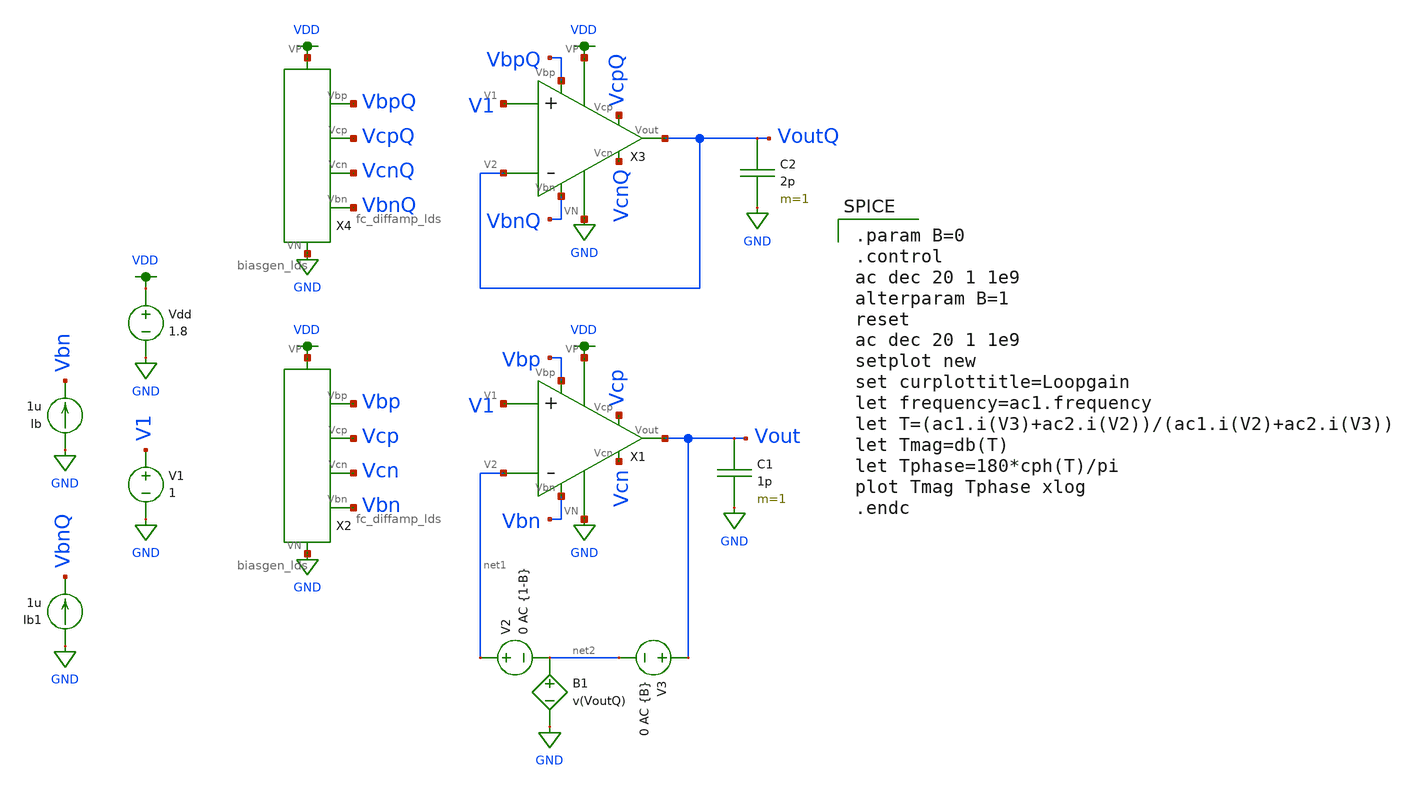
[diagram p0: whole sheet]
** sch_path: fc_diffamp_lg.sch
**.subckt fc_diffamp_lg
Vdd VDD GND 1.8
V1 V1 GND 1
Ib GND Vbn 1u
X1 V1 net1 VDD GND Vout Vbp Vbn Vcp Vcn fc_diffamp_lds
X2 VDD GND Vbn Vcn Vcp Vbp biasgen_lds
C1 Vout GND 1p m=1
Ib1 GND VbnQ 1u
X3 V1 VoutQ VDD GND VoutQ VbpQ VbnQ VcpQ VcnQ fc_diffamp_lds
X4 VDD GND VbnQ VcnQ VcpQ VbpQ biasgen_lds
C2 VoutQ GND 2p m=1
V2 net1 net2 0 AC {1-B}
V3 Vout net2 0 AC {B}
B1 net2 GND V=v(VoutQ)
**** begin user architecture code

.option wnflag=1
.lib ~/skywater/skywater-pdk/libraries/sky130_fd_pr_ngspice/latest/models/sky130.lib.spice tt


.param B=0
.control
ac dec 20 1 1e9
alterparam B=1
reset
ac dec 20 1 1e9
setplot new
set curplottitle=Loopgain
let frequency=ac1.frequency
let T=(ac1.i(V3)+ac2.i(V2))/(ac1.i(V2)+ac2.i(V3))
let Tmag=db(T)
let Tphase=180*cph(T)/pi
plot Tmag Tphase xlog
.endc

**** end user architecture code
**.ends

* expanding   symbol:  /home/madvlsi/Documents/mp3/fc_diffamp_lds.sym # of pins=9
** sym_path: fc_diffamp_lds.sym
** sch_path: fc_diffamp_lds.sch
.subckt fc_diffamp_lds V1 V2 VP VN Vout Vbp Vbn Vcp Vcn
*.ipin V1
*.ipin V2
*.opin Vout
*.iopin VN
*.iopin VP
*.ipin Vcp
*.ipin Vbp
*.ipin Vcn
*.ipin Vbn
XM1a net1 V1 net3 GND sky130_fd_pr__nfet_01v8 L=0.5 W=1.5 nf=1 ad='int((nf+1)/2) * W/nf * 0.29' as='int((nf+2)/2) * W/nf * 0.29'
+ pd='2*int((nf+1)/2) * (W/nf + 0.29)' ps='2*int((nf+2)/2) * (W/nf + 0.29)' nrd='0.29 / W' nrs='0.29 / W'
+ sa=0 sb=0 sd=0 mult=1 m=1
XM2a net1 V2 net2 GND sky130_fd_pr__nfet_01v8 L=0.5 W=1.5 nf=1 ad='int((nf+1)/2) * W/nf * 0.29' as='int((nf+2)/2) * W/nf * 0.29'
+ pd='2*int((nf+1)/2) * (W/nf + 0.29)' ps='2*int((nf+2)/2) * (W/nf + 0.29)' nrd='0.29 / W' nrs='0.29 / W'
+ sa=0 sb=0 sd=0 mult=1 m=1
XM2b net2 V2 net1 GND sky130_fd_pr__nfet_01v8 L=0.5 W=1.5 nf=1 ad='int((nf+1)/2) * W/nf * 0.29' as='int((nf+2)/2) * W/nf * 0.29'
+ pd='2*int((nf+1)/2) * (W/nf + 0.29)' ps='2*int((nf+2)/2) * (W/nf + 0.29)' nrd='0.29 / W' nrs='0.29 / W'
+ sa=0 sb=0 sd=0 mult=1 m=1
XM1b net3 V1 net1 GND sky130_fd_pr__nfet_01v8 L=0.5 W=1.5 nf=1 ad='int((nf+1)/2) * W/nf * 0.29' as='int((nf+2)/2) * W/nf * 0.29'
+ pd='2*int((nf+1)/2) * (W/nf + 0.29)' ps='2*int((nf+2)/2) * (W/nf + 0.29)' nrd='0.29 / W' nrs='0.29 / W'
+ sa=0 sb=0 sd=0 mult=1 m=1
XM1c net1 V1 net3 GND sky130_fd_pr__nfet_01v8 L=0.5 W=1.5 nf=1 ad='int((nf+1)/2) * W/nf * 0.29' as='int((nf+2)/2) * W/nf * 0.29'
+ pd='2*int((nf+1)/2) * (W/nf + 0.29)' ps='2*int((nf+2)/2) * (W/nf + 0.29)' nrd='0.29 / W' nrs='0.29 / W'
+ sa=0 sb=0 sd=0 mult=1 m=1
XM2c net1 V2 net2 GND sky130_fd_pr__nfet_01v8 L=0.5 W=1.5 nf=1 ad='int((nf+1)/2) * W/nf * 0.29' as='int((nf+2)/2) * W/nf * 0.29'
+ pd='2*int((nf+1)/2) * (W/nf + 0.29)' ps='2*int((nf+2)/2) * (W/nf + 0.29)' nrd='0.29 / W' nrs='0.29 / W'
+ sa=0 sb=0 sd=0 mult=1 m=1
XM2d net2 V2 net1 GND sky130_fd_pr__nfet_01v8 L=0.5 W=1.5 nf=1 ad='int((nf+1)/2) * W/nf * 0.29' as='int((nf+2)/2) * W/nf * 0.29'
+ pd='2*int((nf+1)/2) * (W/nf + 0.29)' ps='2*int((nf+2)/2) * (W/nf + 0.29)' nrd='0.29 / W' nrs='0.29 / W'
+ sa=0 sb=0 sd=0 mult=1 m=1
XM1d net3 V1 net1 GND sky130_fd_pr__nfet_01v8 L=0.5 W=1.5 nf=1 ad='int((nf+1)/2) * W/nf * 0.29' as='int((nf+2)/2) * W/nf * 0.29'
+ pd='2*int((nf+1)/2) * (W/nf + 0.29)' ps='2*int((nf+2)/2) * (W/nf + 0.29)' nrd='0.29 / W' nrs='0.29 / W'
+ sa=0 sb=0 sd=0 mult=1 m=1
XM11a net1 Vbn VN GND sky130_fd_pr__nfet_01v8 L=0.5 W=1.5 nf=1 ad='int((nf+1)/2) * W/nf * 0.29' as='int((nf+2)/2) * W/nf * 0.29'
+ pd='2*int((nf+1)/2) * (W/nf + 0.29)' ps='2*int((nf+2)/2) * (W/nf + 0.29)' nrd='0.29 / W' nrs='0.29 / W'
+ sa=0 sb=0 sd=0 mult=1 m=1
XM12a VN Vbn Vbn GND sky130_fd_pr__nfet_01v8 L=0.5 W=1.5 nf=1 ad='int((nf+1)/2) * W/nf * 0.29' as='int((nf+2)/2) * W/nf * 0.29'
+ pd='2*int((nf+1)/2) * (W/nf + 0.29)' ps='2*int((nf+2)/2) * (W/nf + 0.29)' nrd='0.29 / W' nrs='0.29 / W'
+ sa=0 sb=0 sd=0 mult=1 m=1
XM12b Vbn Vbn VN GND sky130_fd_pr__nfet_01v8 L=0.5 W=1.5 nf=1 ad='int((nf+1)/2) * W/nf * 0.29' as='int((nf+2)/2) * W/nf * 0.29'
+ pd='2*int((nf+1)/2) * (W/nf + 0.29)' ps='2*int((nf+2)/2) * (W/nf + 0.29)' nrd='0.29 / W' nrs='0.29 / W'
+ sa=0 sb=0 sd=0 mult=1 m=1
XM11b VN Vbn net1 GND sky130_fd_pr__nfet_01v8 L=0.5 W=1.5 nf=1 ad='int((nf+1)/2) * W/nf * 0.29' as='int((nf+2)/2) * W/nf * 0.29'
+ pd='2*int((nf+1)/2) * (W/nf + 0.29)' ps='2*int((nf+2)/2) * (W/nf + 0.29)' nrd='0.29 / W' nrs='0.29 / W'
+ sa=0 sb=0 sd=0 mult=1 m=1
XM11c net1 Vbn VN GND sky130_fd_pr__nfet_01v8 L=0.5 W=1.5 nf=1 ad='int((nf+1)/2) * W/nf * 0.29' as='int((nf+2)/2) * W/nf * 0.29'
+ pd='2*int((nf+1)/2) * (W/nf + 0.29)' ps='2*int((nf+2)/2) * (W/nf + 0.29)' nrd='0.29 / W' nrs='0.29 / W'
+ sa=0 sb=0 sd=0 mult=1 m=1
XM12c VN Vbn Vbn GND sky130_fd_pr__nfet_01v8 L=0.5 W=1.5 nf=1 ad='int((nf+1)/2) * W/nf * 0.29' as='int((nf+2)/2) * W/nf * 0.29'
+ pd='2*int((nf+1)/2) * (W/nf + 0.29)' ps='2*int((nf+2)/2) * (W/nf + 0.29)' nrd='0.29 / W' nrs='0.29 / W'
+ sa=0 sb=0 sd=0 mult=1 m=1
XM12d Vbn Vbn VN GND sky130_fd_pr__nfet_01v8 L=0.5 W=1.5 nf=1 ad='int((nf+1)/2) * W/nf * 0.29' as='int((nf+2)/2) * W/nf * 0.29'
+ pd='2*int((nf+1)/2) * (W/nf + 0.29)' ps='2*int((nf+2)/2) * (W/nf + 0.29)' nrd='0.29 / W' nrs='0.29 / W'
+ sa=0 sb=0 sd=0 mult=1 m=1
XM11d VN Vbn net1 GND sky130_fd_pr__nfet_01v8 L=0.5 W=1.5 nf=1 ad='int((nf+1)/2) * W/nf * 0.29' as='int((nf+2)/2) * W/nf * 0.29'
+ pd='2*int((nf+1)/2) * (W/nf + 0.29)' ps='2*int((nf+2)/2) * (W/nf + 0.29)' nrd='0.29 / W' nrs='0.29 / W'
+ sa=0 sb=0 sd=0 mult=1 m=1
XM9a net4 Vcn net8 GND sky130_fd_pr__nfet_01v8 L=0.5 W=3 nf=1 ad='int((nf+1)/2) * W/nf * 0.29' as='int((nf+2)/2) * W/nf * 0.29'
+ pd='2*int((nf+1)/2) * (W/nf + 0.29)' ps='2*int((nf+2)/2) * (W/nf + 0.29)' nrd='0.29 / W' nrs='0.29 / W'
+ sa=0 sb=0 sd=0 mult=1 m=1
XM7a net4 net8 VN GND sky130_fd_pr__nfet_01v8 L=0.5 W=3 nf=1 ad='int((nf+1)/2) * W/nf * 0.29' as='int((nf+2)/2) * W/nf * 0.29'
+ pd='2*int((nf+1)/2) * (W/nf + 0.29)' ps='2*int((nf+2)/2) * (W/nf + 0.29)' nrd='0.29 / W' nrs='0.29 / W'
+ sa=0 sb=0 sd=0 mult=1 m=1
XM8a VN net8 net5 GND sky130_fd_pr__nfet_01v8 L=0.5 W=3 nf=1 ad='int((nf+1)/2) * W/nf * 0.29' as='int((nf+2)/2) * W/nf * 0.29'
+ pd='2*int((nf+1)/2) * (W/nf + 0.29)' ps='2*int((nf+2)/2) * (W/nf + 0.29)' nrd='0.29 / W' nrs='0.29 / W'
+ sa=0 sb=0 sd=0 mult=1 m=1
XM10a Vout Vcn net5 GND sky130_fd_pr__nfet_01v8 L=0.5 W=3 nf=1 ad='int((nf+1)/2) * W/nf * 0.29' as='int((nf+2)/2) * W/nf * 0.29'
+ pd='2*int((nf+1)/2) * (W/nf + 0.29)' ps='2*int((nf+2)/2) * (W/nf + 0.29)' nrd='0.29 / W' nrs='0.29 / W'
+ sa=0 sb=0 sd=0 mult=1 m=1
XM10b net6 Vcn Vout GND sky130_fd_pr__nfet_01v8 L=0.5 W=3 nf=1 ad='int((nf+1)/2) * W/nf * 0.29' as='int((nf+2)/2) * W/nf * 0.29'
+ pd='2*int((nf+1)/2) * (W/nf + 0.29)' ps='2*int((nf+2)/2) * (W/nf + 0.29)' nrd='0.29 / W' nrs='0.29 / W'
+ sa=0 sb=0 sd=0 mult=1 m=1
XM9b net8 Vcn net7 GND sky130_fd_pr__nfet_01v8 L=0.5 W=3 nf=1 ad='int((nf+1)/2) * W/nf * 0.29' as='int((nf+2)/2) * W/nf * 0.29'
+ pd='2*int((nf+1)/2) * (W/nf + 0.29)' ps='2*int((nf+2)/2) * (W/nf + 0.29)' nrd='0.29 / W' nrs='0.29 / W'
+ sa=0 sb=0 sd=0 mult=1 m=1
XM7b VN net8 net7 GND sky130_fd_pr__nfet_01v8 L=0.5 W=3 nf=1 ad='int((nf+1)/2) * W/nf * 0.29' as='int((nf+2)/2) * W/nf * 0.29'
+ pd='2*int((nf+1)/2) * (W/nf + 0.29)' ps='2*int((nf+2)/2) * (W/nf + 0.29)' nrd='0.29 / W' nrs='0.29 / W'
+ sa=0 sb=0 sd=0 mult=1 m=1
XM8b net6 net8 VN GND sky130_fd_pr__nfet_01v8 L=0.5 W=3 nf=1 ad='int((nf+1)/2) * W/nf * 0.29' as='int((nf+2)/2) * W/nf * 0.29'
+ pd='2*int((nf+1)/2) * (W/nf + 0.29)' ps='2*int((nf+2)/2) * (W/nf + 0.29)' nrd='0.29 / W' nrs='0.29 / W'
+ sa=0 sb=0 sd=0 mult=1 m=1
XM9c net9 Vcn net8 GND sky130_fd_pr__nfet_01v8 L=0.5 W=3 nf=1 ad='int((nf+1)/2) * W/nf * 0.29' as='int((nf+2)/2) * W/nf * 0.29'
+ pd='2*int((nf+1)/2) * (W/nf + 0.29)' ps='2*int((nf+2)/2) * (W/nf + 0.29)' nrd='0.29 / W' nrs='0.29 / W'
+ sa=0 sb=0 sd=0 mult=1 m=1
XM7c net9 net8 VN GND sky130_fd_pr__nfet_01v8 L=0.5 W=3 nf=1 ad='int((nf+1)/2) * W/nf * 0.29' as='int((nf+2)/2) * W/nf * 0.29'
+ pd='2*int((nf+1)/2) * (W/nf + 0.29)' ps='2*int((nf+2)/2) * (W/nf + 0.29)' nrd='0.29 / W' nrs='0.29 / W'
+ sa=0 sb=0 sd=0 mult=1 m=1
XM8c VN net8 net10 GND sky130_fd_pr__nfet_01v8 L=0.5 W=3 nf=1 ad='int((nf+1)/2) * W/nf * 0.29' as='int((nf+2)/2) * W/nf * 0.29'
+ pd='2*int((nf+1)/2) * (W/nf + 0.29)' ps='2*int((nf+2)/2) * (W/nf + 0.29)' nrd='0.29 / W' nrs='0.29 / W'
+ sa=0 sb=0 sd=0 mult=1 m=1
XM10c Vout Vcn net10 GND sky130_fd_pr__nfet_01v8 L=0.5 W=3 nf=1 ad='int((nf+1)/2) * W/nf * 0.29' as='int((nf+2)/2) * W/nf * 0.29'
+ pd='2*int((nf+1)/2) * (W/nf + 0.29)' ps='2*int((nf+2)/2) * (W/nf + 0.29)' nrd='0.29 / W' nrs='0.29 / W'
+ sa=0 sb=0 sd=0 mult=1 m=1
XM10d net11 Vcn Vout GND sky130_fd_pr__nfet_01v8 L=0.5 W=3 nf=1 ad='int((nf+1)/2) * W/nf * 0.29' as='int((nf+2)/2) * W/nf * 0.29'
+ pd='2*int((nf+1)/2) * (W/nf + 0.29)' ps='2*int((nf+2)/2) * (W/nf + 0.29)' nrd='0.29 / W' nrs='0.29 / W'
+ sa=0 sb=0 sd=0 mult=1 m=1
XM9d net8 Vcn net12 GND sky130_fd_pr__nfet_01v8 L=0.5 W=3 nf=1 ad='int((nf+1)/2) * W/nf * 0.29' as='int((nf+2)/2) * W/nf * 0.29'
+ pd='2*int((nf+1)/2) * (W/nf + 0.29)' ps='2*int((nf+2)/2) * (W/nf + 0.29)' nrd='0.29 / W' nrs='0.29 / W'
+ sa=0 sb=0 sd=0 mult=1 m=1
XM7d VN net8 net12 GND sky130_fd_pr__nfet_01v8 L=0.5 W=3 nf=1 ad='int((nf+1)/2) * W/nf * 0.29' as='int((nf+2)/2) * W/nf * 0.29'
+ pd='2*int((nf+1)/2) * (W/nf + 0.29)' ps='2*int((nf+2)/2) * (W/nf + 0.29)' nrd='0.29 / W' nrs='0.29 / W'
+ sa=0 sb=0 sd=0 mult=1 m=1
XM8d net11 net8 VN GND sky130_fd_pr__nfet_01v8 L=0.5 W=3 nf=1 ad='int((nf+1)/2) * W/nf * 0.29' as='int((nf+2)/2) * W/nf * 0.29'
+ pd='2*int((nf+1)/2) * (W/nf + 0.29)' ps='2*int((nf+2)/2) * (W/nf + 0.29)' nrd='0.29 / W' nrs='0.29 / W'
+ sa=0 sb=0 sd=0 mult=1 m=1
XM5a net8 Vcp net3 VDD sky130_fd_pr__pfet_01v8 L=0.5 W=3 nf=1 ad='int((nf+1)/2) * W/nf * 0.29' as='int((nf+2)/2) * W/nf * 0.29'
+ pd='2*int((nf+1)/2) * (W/nf + 0.29)' ps='2*int((nf+2)/2) * (W/nf + 0.29)' nrd='0.29 / W' nrs='0.29 / W'
+ sa=0 sb=0 sd=0 mult=1 m=1
XM5b net3 Vcp net8 VDD sky130_fd_pr__pfet_01v8 L=0.5 W=3 nf=1 ad='int((nf+1)/2) * W/nf * 0.29' as='int((nf+2)/2) * W/nf * 0.29'
+ pd='2*int((nf+1)/2) * (W/nf + 0.29)' ps='2*int((nf+2)/2) * (W/nf + 0.29)' nrd='0.29 / W' nrs='0.29 / W'
+ sa=0 sb=0 sd=0 mult=1 m=1
XM5c net8 Vcp net3 VDD sky130_fd_pr__pfet_01v8 L=0.5 W=3 nf=1 ad='int((nf+1)/2) * W/nf * 0.29' as='int((nf+2)/2) * W/nf * 0.29'
+ pd='2*int((nf+1)/2) * (W/nf + 0.29)' ps='2*int((nf+2)/2) * (W/nf + 0.29)' nrd='0.29 / W' nrs='0.29 / W'
+ sa=0 sb=0 sd=0 mult=1 m=1
XM5d net3 Vcp net8 VDD sky130_fd_pr__pfet_01v8 L=0.5 W=3 nf=1 ad='int((nf+1)/2) * W/nf * 0.29' as='int((nf+2)/2) * W/nf * 0.29'
+ pd='2*int((nf+1)/2) * (W/nf + 0.29)' ps='2*int((nf+2)/2) * (W/nf + 0.29)' nrd='0.29 / W' nrs='0.29 / W'
+ sa=0 sb=0 sd=0 mult=1 m=1
XM6a net2 Vcp Vout VDD sky130_fd_pr__pfet_01v8 L=0.5 W=3 nf=1 ad='int((nf+1)/2) * W/nf * 0.29' as='int((nf+2)/2) * W/nf * 0.29'
+ pd='2*int((nf+1)/2) * (W/nf + 0.29)' ps='2*int((nf+2)/2) * (W/nf + 0.29)' nrd='0.29 / W' nrs='0.29 / W'
+ sa=0 sb=0 sd=0 mult=1 m=1
XM6b Vout Vcp net2 VDD sky130_fd_pr__pfet_01v8 L=0.5 W=3 nf=1 ad='int((nf+1)/2) * W/nf * 0.29' as='int((nf+2)/2) * W/nf * 0.29'
+ pd='2*int((nf+1)/2) * (W/nf + 0.29)' ps='2*int((nf+2)/2) * (W/nf + 0.29)' nrd='0.29 / W' nrs='0.29 / W'
+ sa=0 sb=0 sd=0 mult=1 m=1
XM6c net2 Vcp Vout VDD sky130_fd_pr__pfet_01v8 L=0.5 W=3 nf=1 ad='int((nf+1)/2) * W/nf * 0.29' as='int((nf+2)/2) * W/nf * 0.29'
+ pd='2*int((nf+1)/2) * (W/nf + 0.29)' ps='2*int((nf+2)/2) * (W/nf + 0.29)' nrd='0.29 / W' nrs='0.29 / W'
+ sa=0 sb=0 sd=0 mult=1 m=1
XM6d Vout Vcp net2 VDD sky130_fd_pr__pfet_01v8 L=0.5 W=3 nf=1 ad='int((nf+1)/2) * W/nf * 0.29' as='int((nf+2)/2) * W/nf * 0.29'
+ pd='2*int((nf+1)/2) * (W/nf + 0.29)' ps='2*int((nf+2)/2) * (W/nf + 0.29)' nrd='0.29 / W' nrs='0.29 / W'
+ sa=0 sb=0 sd=0 mult=1 m=1
XM3a VP Vbp net3 VDD sky130_fd_pr__pfet_01v8 L=0.5 W=3 nf=1 ad='int((nf+1)/2) * W/nf * 0.29' as='int((nf+2)/2) * W/nf * 0.29'
+ pd='2*int((nf+1)/2) * (W/nf + 0.29)' ps='2*int((nf+2)/2) * (W/nf + 0.29)' nrd='0.29 / W' nrs='0.29 / W'
+ sa=0 sb=0 sd=0 mult=1 m=1
XM3b net3 Vbp VP VDD sky130_fd_pr__pfet_01v8 L=0.5 W=3 nf=1 ad='int((nf+1)/2) * W/nf * 0.29' as='int((nf+2)/2) * W/nf * 0.29'
+ pd='2*int((nf+1)/2) * (W/nf + 0.29)' ps='2*int((nf+2)/2) * (W/nf + 0.29)' nrd='0.29 / W' nrs='0.29 / W'
+ sa=0 sb=0 sd=0 mult=1 m=1
XM3c VP Vbp net3 VDD sky130_fd_pr__pfet_01v8 L=0.5 W=3 nf=1 ad='int((nf+1)/2) * W/nf * 0.29' as='int((nf+2)/2) * W/nf * 0.29'
+ pd='2*int((nf+1)/2) * (W/nf + 0.29)' ps='2*int((nf+2)/2) * (W/nf + 0.29)' nrd='0.29 / W' nrs='0.29 / W'
+ sa=0 sb=0 sd=0 mult=1 m=1
XM3d net3 Vbp VP VDD sky130_fd_pr__pfet_01v8 L=0.5 W=3 nf=1 ad='int((nf+1)/2) * W/nf * 0.29' as='int((nf+2)/2) * W/nf * 0.29'
+ pd='2*int((nf+1)/2) * (W/nf + 0.29)' ps='2*int((nf+2)/2) * (W/nf + 0.29)' nrd='0.29 / W' nrs='0.29 / W'
+ sa=0 sb=0 sd=0 mult=1 m=1
XM4a net2 Vbp VP VDD sky130_fd_pr__pfet_01v8 L=0.5 W=3 nf=1 ad='int((nf+1)/2) * W/nf * 0.29' as='int((nf+2)/2) * W/nf * 0.29'
+ pd='2*int((nf+1)/2) * (W/nf + 0.29)' ps='2*int((nf+2)/2) * (W/nf + 0.29)' nrd='0.29 / W' nrs='0.29 / W'
+ sa=0 sb=0 sd=0 mult=1 m=1
XM4b VP Vbp net2 VDD sky130_fd_pr__pfet_01v8 L=0.5 W=3 nf=1 ad='int((nf+1)/2) * W/nf * 0.29' as='int((nf+2)/2) * W/nf * 0.29'
+ pd='2*int((nf+1)/2) * (W/nf + 0.29)' ps='2*int((nf+2)/2) * (W/nf + 0.29)' nrd='0.29 / W' nrs='0.29 / W'
+ sa=0 sb=0 sd=0 mult=1 m=1
XM4c net2 Vbp VP VDD sky130_fd_pr__pfet_01v8 L=0.5 W=3 nf=1 ad='int((nf+1)/2) * W/nf * 0.29' as='int((nf+2)/2) * W/nf * 0.29'
+ pd='2*int((nf+1)/2) * (W/nf + 0.29)' ps='2*int((nf+2)/2) * (W/nf + 0.29)' nrd='0.29 / W' nrs='0.29 / W'
+ sa=0 sb=0 sd=0 mult=1 m=1
XM4d VP Vbp net2 VDD sky130_fd_pr__pfet_01v8 L=0.5 W=3 nf=1 ad='int((nf+1)/2) * W/nf * 0.29' as='int((nf+2)/2) * W/nf * 0.29'
+ pd='2*int((nf+1)/2) * (W/nf + 0.29)' ps='2*int((nf+2)/2) * (W/nf + 0.29)' nrd='0.29 / W' nrs='0.29 / W'
+ sa=0 sb=0 sd=0 mult=1 m=1
XM13 VN VN net3 GND sky130_fd_pr__nfet_01v8 L=0.5 W=1.5 nf=1 ad='int((nf+1)/2) * W/nf * 0.29' as='int((nf+2)/2) * W/nf * 0.29'
+ pd='2*int((nf+1)/2) * (W/nf + 0.29)' ps='2*int((nf+2)/2) * (W/nf + 0.29)' nrd='0.29 / W' nrs='0.29 / W'
+ sa=0 sb=0 sd=0 mult=1 m=1
XM15 VN VN net8 GND sky130_fd_pr__nfet_01v8 L=0.5 W=3 nf=1 ad='int((nf+1)/2) * W/nf * 0.29' as='int((nf+2)/2) * W/nf * 0.29'
+ pd='2*int((nf+1)/2) * (W/nf + 0.29)' ps='2*int((nf+2)/2) * (W/nf + 0.29)' nrd='0.29 / W' nrs='0.29 / W'
+ sa=0 sb=0 sd=0 mult=1 m=1
XM17 Vbn VN VN GND sky130_fd_pr__nfet_01v8 L=0.5 W=1.5 nf=1 ad='int((nf+1)/2) * W/nf * 0.29' as='int((nf+2)/2) * W/nf * 0.29'
+ pd='2*int((nf+1)/2) * (W/nf + 0.29)' ps='2*int((nf+2)/2) * (W/nf + 0.29)' nrd='0.29 / W' nrs='0.29 / W'
+ sa=0 sb=0 sd=0 mult=1 m=1
XM18 net8 VN VN GND sky130_fd_pr__nfet_01v8 L=0.5 W=3 nf=1 ad='int((nf+1)/2) * W/nf * 0.29' as='int((nf+2)/2) * W/nf * 0.29'
+ pd='2*int((nf+1)/2) * (W/nf + 0.29)' ps='2*int((nf+2)/2) * (W/nf + 0.29)' nrd='0.29 / W' nrs='0.29 / W'
+ sa=0 sb=0 sd=0 mult=1 m=1
XM19 VP VP net8 VDD sky130_fd_pr__pfet_01v8 L=0.5 W=3 nf=1 ad='int((nf+1)/2) * W/nf * 0.29' as='int((nf+2)/2) * W/nf * 0.29'
+ pd='2*int((nf+1)/2) * (W/nf + 0.29)' ps='2*int((nf+2)/2) * (W/nf + 0.29)' nrd='0.29 / W' nrs='0.29 / W'
+ sa=0 sb=0 sd=0 mult=1 m=1
XM20 net8 VP VP VDD sky130_fd_pr__pfet_01v8 L=0.5 W=3 nf=1 ad='int((nf+1)/2) * W/nf * 0.29' as='int((nf+2)/2) * W/nf * 0.29'
+ pd='2*int((nf+1)/2) * (W/nf + 0.29)' ps='2*int((nf+2)/2) * (W/nf + 0.29)' nrd='0.29 / W' nrs='0.29 / W'
+ sa=0 sb=0 sd=0 mult=1 m=1
XM1e net1 V1 net3 GND sky130_fd_pr__nfet_01v8 L=0.5 W=1.5 nf=1 ad='int((nf+1)/2) * W/nf * 0.29' as='int((nf+2)/2) * W/nf * 0.29'
+ pd='2*int((nf+1)/2) * (W/nf + 0.29)' ps='2*int((nf+2)/2) * (W/nf + 0.29)' nrd='0.29 / W' nrs='0.29 / W'
+ sa=0 sb=0 sd=0 mult=1 m=1
XM2e net1 V2 net2 GND sky130_fd_pr__nfet_01v8 L=0.5 W=1.5 nf=1 ad='int((nf+1)/2) * W/nf * 0.29' as='int((nf+2)/2) * W/nf * 0.29'
+ pd='2*int((nf+1)/2) * (W/nf + 0.29)' ps='2*int((nf+2)/2) * (W/nf + 0.29)' nrd='0.29 / W' nrs='0.29 / W'
+ sa=0 sb=0 sd=0 mult=1 m=1
XM2f net2 V2 net1 GND sky130_fd_pr__nfet_01v8 L=0.5 W=1.5 nf=1 ad='int((nf+1)/2) * W/nf * 0.29' as='int((nf+2)/2) * W/nf * 0.29'
+ pd='2*int((nf+1)/2) * (W/nf + 0.29)' ps='2*int((nf+2)/2) * (W/nf + 0.29)' nrd='0.29 / W' nrs='0.29 / W'
+ sa=0 sb=0 sd=0 mult=1 m=1
XM1f net3 V1 net1 GND sky130_fd_pr__nfet_01v8 L=0.5 W=1.5 nf=1 ad='int((nf+1)/2) * W/nf * 0.29' as='int((nf+2)/2) * W/nf * 0.29'
+ pd='2*int((nf+1)/2) * (W/nf + 0.29)' ps='2*int((nf+2)/2) * (W/nf + 0.29)' nrd='0.29 / W' nrs='0.29 / W'
+ sa=0 sb=0 sd=0 mult=1 m=1
XM1g net1 V1 net3 GND sky130_fd_pr__nfet_01v8 L=0.5 W=1.5 nf=1 ad='int((nf+1)/2) * W/nf * 0.29' as='int((nf+2)/2) * W/nf * 0.29'
+ pd='2*int((nf+1)/2) * (W/nf + 0.29)' ps='2*int((nf+2)/2) * (W/nf + 0.29)' nrd='0.29 / W' nrs='0.29 / W'
+ sa=0 sb=0 sd=0 mult=1 m=1
XM2g net1 V2 net2 GND sky130_fd_pr__nfet_01v8 L=0.5 W=1.5 nf=1 ad='int((nf+1)/2) * W/nf * 0.29' as='int((nf+2)/2) * W/nf * 0.29'
+ pd='2*int((nf+1)/2) * (W/nf + 0.29)' ps='2*int((nf+2)/2) * (W/nf + 0.29)' nrd='0.29 / W' nrs='0.29 / W'
+ sa=0 sb=0 sd=0 mult=1 m=1
XM2h net2 V2 net1 GND sky130_fd_pr__nfet_01v8 L=0.5 W=1.5 nf=1 ad='int((nf+1)/2) * W/nf * 0.29' as='int((nf+2)/2) * W/nf * 0.29'
+ pd='2*int((nf+1)/2) * (W/nf + 0.29)' ps='2*int((nf+2)/2) * (W/nf + 0.29)' nrd='0.29 / W' nrs='0.29 / W'
+ sa=0 sb=0 sd=0 mult=1 m=1
XM1h net3 V1 net1 GND sky130_fd_pr__nfet_01v8 L=0.5 W=1.5 nf=1 ad='int((nf+1)/2) * W/nf * 0.29' as='int((nf+2)/2) * W/nf * 0.29'
+ pd='2*int((nf+1)/2) * (W/nf + 0.29)' ps='2*int((nf+2)/2) * (W/nf + 0.29)' nrd='0.29 / W' nrs='0.29 / W'
+ sa=0 sb=0 sd=0 mult=1 m=1
XM16 net3 VN VN GND sky130_fd_pr__nfet_01v8 L=0.5 W=1.5 nf=1 ad='int((nf+1)/2) * W/nf * 0.29' as='int((nf+2)/2) * W/nf * 0.29'
+ pd='2*int((nf+1)/2) * (W/nf + 0.29)' ps='2*int((nf+2)/2) * (W/nf + 0.29)' nrd='0.29 / W' nrs='0.29 / W'
+ sa=0 sb=0 sd=0 mult=1 m=1
XM11e net1 Vbn VN GND sky130_fd_pr__nfet_01v8 L=0.5 W=1.5 nf=1 ad='int((nf+1)/2) * W/nf * 0.29' as='int((nf+2)/2) * W/nf * 0.29'
+ pd='2*int((nf+1)/2) * (W/nf + 0.29)' ps='2*int((nf+2)/2) * (W/nf + 0.29)' nrd='0.29 / W' nrs='0.29 / W'
+ sa=0 sb=0 sd=0 mult=1 m=1
XM12e VN Vbn Vbn GND sky130_fd_pr__nfet_01v8 L=0.5 W=1.5 nf=1 ad='int((nf+1)/2) * W/nf * 0.29' as='int((nf+2)/2) * W/nf * 0.29'
+ pd='2*int((nf+1)/2) * (W/nf + 0.29)' ps='2*int((nf+2)/2) * (W/nf + 0.29)' nrd='0.29 / W' nrs='0.29 / W'
+ sa=0 sb=0 sd=0 mult=1 m=1
XM12f Vbn Vbn VN GND sky130_fd_pr__nfet_01v8 L=0.5 W=1.5 nf=1 ad='int((nf+1)/2) * W/nf * 0.29' as='int((nf+2)/2) * W/nf * 0.29'
+ pd='2*int((nf+1)/2) * (W/nf + 0.29)' ps='2*int((nf+2)/2) * (W/nf + 0.29)' nrd='0.29 / W' nrs='0.29 / W'
+ sa=0 sb=0 sd=0 mult=1 m=1
XM11f VN Vbn net1 GND sky130_fd_pr__nfet_01v8 L=0.5 W=1.5 nf=1 ad='int((nf+1)/2) * W/nf * 0.29' as='int((nf+2)/2) * W/nf * 0.29'
+ pd='2*int((nf+1)/2) * (W/nf + 0.29)' ps='2*int((nf+2)/2) * (W/nf + 0.29)' nrd='0.29 / W' nrs='0.29 / W'
+ sa=0 sb=0 sd=0 mult=1 m=1
XM11g net1 Vbn VN GND sky130_fd_pr__nfet_01v8 L=0.5 W=1.5 nf=1 ad='int((nf+1)/2) * W/nf * 0.29' as='int((nf+2)/2) * W/nf * 0.29'
+ pd='2*int((nf+1)/2) * (W/nf + 0.29)' ps='2*int((nf+2)/2) * (W/nf + 0.29)' nrd='0.29 / W' nrs='0.29 / W'
+ sa=0 sb=0 sd=0 mult=1 m=1
XM12g VN Vbn Vbn GND sky130_fd_pr__nfet_01v8 L=0.5 W=1.5 nf=1 ad='int((nf+1)/2) * W/nf * 0.29' as='int((nf+2)/2) * W/nf * 0.29'
+ pd='2*int((nf+1)/2) * (W/nf + 0.29)' ps='2*int((nf+2)/2) * (W/nf + 0.29)' nrd='0.29 / W' nrs='0.29 / W'
+ sa=0 sb=0 sd=0 mult=1 m=1
XM12h Vbn Vbn VN GND sky130_fd_pr__nfet_01v8 L=0.5 W=1.5 nf=1 ad='int((nf+1)/2) * W/nf * 0.29' as='int((nf+2)/2) * W/nf * 0.29'
+ pd='2*int((nf+1)/2) * (W/nf + 0.29)' ps='2*int((nf+2)/2) * (W/nf + 0.29)' nrd='0.29 / W' nrs='0.29 / W'
+ sa=0 sb=0 sd=0 mult=1 m=1
XM11h VN Vbn net1 GND sky130_fd_pr__nfet_01v8 L=0.5 W=1.5 nf=1 ad='int((nf+1)/2) * W/nf * 0.29' as='int((nf+2)/2) * W/nf * 0.29'
+ pd='2*int((nf+1)/2) * (W/nf + 0.29)' ps='2*int((nf+2)/2) * (W/nf + 0.29)' nrd='0.29 / W' nrs='0.29 / W'
+ sa=0 sb=0 sd=0 mult=1 m=1
XM14 VN VN Vbn GND sky130_fd_pr__nfet_01v8 L=0.5 W=1.5 nf=1 ad='int((nf+1)/2) * W/nf * 0.29' as='int((nf+2)/2) * W/nf * 0.29'
+ pd='2*int((nf+1)/2) * (W/nf + 0.29)' ps='2*int((nf+2)/2) * (W/nf + 0.29)' nrd='0.29 / W' nrs='0.29 / W'
+ sa=0 sb=0 sd=0 mult=1 m=1
.ends


* expanding   symbol:  /home/madvlsi/Documents/mp3/biasgen_lds.sym # of pins=6
** sym_path: biasgen_lds.sym
** sch_path: biasgen_lds.sch
.subckt biasgen_lds VP VN Vbn Vcn Vcp Vbp
*.opin Vbp
*.iopin VP
*.opin Vcp
*.opin Vcn
*.ipin Vbn
*.iopin VN
XM2a Vcn Vbp VP VDD sky130_fd_pr__pfet_01v8 L=0.5 W=6 nf=1 ad='int((nf+1)/2) * W/nf * 0.29' as='int((nf+2)/2) * W/nf * 0.29'
+ pd='2*int((nf+1)/2) * (W/nf + 0.29)' ps='2*int((nf+2)/2) * (W/nf + 0.29)' nrd='0.29 / W' nrs='0.29 / W'
+ sa=0 sb=0 sd=0 mult=1 m=1
XM1a VP Vbp net1 VDD sky130_fd_pr__pfet_01v8 L=0.5 W=6 nf=1 ad='int((nf+1)/2) * W/nf * 0.29' as='int((nf+2)/2) * W/nf * 0.29'
+ pd='2*int((nf+1)/2) * (W/nf + 0.29)' ps='2*int((nf+2)/2) * (W/nf + 0.29)' nrd='0.29 / W' nrs='0.29 / W'
+ sa=0 sb=0 sd=0 mult=1 m=1
XM1b net1 Vbp net2 VDD sky130_fd_pr__pfet_01v8 L=0.5 W=6 nf=1 ad='int((nf+1)/2) * W/nf * 0.29' as='int((nf+2)/2) * W/nf * 0.29'
+ pd='2*int((nf+1)/2) * (W/nf + 0.29)' ps='2*int((nf+2)/2) * (W/nf + 0.29)' nrd='0.29 / W' nrs='0.29 / W'
+ sa=0 sb=0 sd=0 mult=1 m=1
XM1c net2 Vbp net3 VDD sky130_fd_pr__pfet_01v8 L=0.5 W=6 nf=1 ad='int((nf+1)/2) * W/nf * 0.29' as='int((nf+2)/2) * W/nf * 0.29'
+ pd='2*int((nf+1)/2) * (W/nf + 0.29)' ps='2*int((nf+2)/2) * (W/nf + 0.29)' nrd='0.29 / W' nrs='0.29 / W'
+ sa=0 sb=0 sd=0 mult=1 m=1
XM1d net3 Vbp net4 VDD sky130_fd_pr__pfet_01v8 L=0.5 W=6 nf=1 ad='int((nf+1)/2) * W/nf * 0.29' as='int((nf+2)/2) * W/nf * 0.29'
+ pd='2*int((nf+1)/2) * (W/nf + 0.29)' ps='2*int((nf+2)/2) * (W/nf + 0.29)' nrd='0.29 / W' nrs='0.29 / W'
+ sa=0 sb=0 sd=0 mult=1 m=1
XM1e net4 Vbp net5 VDD sky130_fd_pr__pfet_01v8 L=0.5 W=6 nf=1 ad='int((nf+1)/2) * W/nf * 0.29' as='int((nf+2)/2) * W/nf * 0.29'
+ pd='2*int((nf+1)/2) * (W/nf + 0.29)' ps='2*int((nf+2)/2) * (W/nf + 0.29)' nrd='0.29 / W' nrs='0.29 / W'
+ sa=0 sb=0 sd=0 mult=1 m=1
XM1f net5 Vbp net14 VDD sky130_fd_pr__pfet_01v8 L=0.5 W=6 nf=1 ad='int((nf+1)/2) * W/nf * 0.29' as='int((nf+2)/2) * W/nf * 0.29'
+ pd='2*int((nf+1)/2) * (W/nf + 0.29)' ps='2*int((nf+2)/2) * (W/nf + 0.29)' nrd='0.29 / W' nrs='0.29 / W'
+ sa=0 sb=0 sd=0 mult=1 m=1
XM1g net14 Vbp net6 VDD sky130_fd_pr__pfet_01v8 L=0.5 W=6 nf=1 ad='int((nf+1)/2) * W/nf * 0.29' as='int((nf+2)/2) * W/nf * 0.29'
+ pd='2*int((nf+1)/2) * (W/nf + 0.29)' ps='2*int((nf+2)/2) * (W/nf + 0.29)' nrd='0.29 / W' nrs='0.29 / W'
+ sa=0 sb=0 sd=0 mult=1 m=1
XM1h net6 Vbp net7 VDD sky130_fd_pr__pfet_01v8 L=0.5 W=6 nf=1 ad='int((nf+1)/2) * W/nf * 0.29' as='int((nf+2)/2) * W/nf * 0.29'
+ pd='2*int((nf+1)/2) * (W/nf + 0.29)' ps='2*int((nf+2)/2) * (W/nf + 0.29)' nrd='0.29 / W' nrs='0.29 / W'
+ sa=0 sb=0 sd=0 mult=1 m=1
XM1i net7 Vbp net8 VDD sky130_fd_pr__pfet_01v8 L=0.5 W=6 nf=1 ad='int((nf+1)/2) * W/nf * 0.29' as='int((nf+2)/2) * W/nf * 0.29'
+ pd='2*int((nf+1)/2) * (W/nf + 0.29)' ps='2*int((nf+2)/2) * (W/nf + 0.29)' nrd='0.29 / W' nrs='0.29 / W'
+ sa=0 sb=0 sd=0 mult=1 m=1
XM1j net8 Vbp net9 VDD sky130_fd_pr__pfet_01v8 L=0.5 W=6 nf=1 ad='int((nf+1)/2) * W/nf * 0.29' as='int((nf+2)/2) * W/nf * 0.29'
+ pd='2*int((nf+1)/2) * (W/nf + 0.29)' ps='2*int((nf+2)/2) * (W/nf + 0.29)' nrd='0.29 / W' nrs='0.29 / W'
+ sa=0 sb=0 sd=0 mult=1 m=1
XM1k net9 Vbp net10 VDD sky130_fd_pr__pfet_01v8 L=0.5 W=6 nf=1 ad='int((nf+1)/2) * W/nf * 0.29' as='int((nf+2)/2) * W/nf * 0.29'
+ pd='2*int((nf+1)/2) * (W/nf + 0.29)' ps='2*int((nf+2)/2) * (W/nf + 0.29)' nrd='0.29 / W' nrs='0.29 / W'
+ sa=0 sb=0 sd=0 mult=1 m=1
XM1l net10 Vbp VP VDD sky130_fd_pr__pfet_01v8 L=0.5 W=6 nf=1 ad='int((nf+1)/2) * W/nf * 0.29' as='int((nf+2)/2) * W/nf * 0.29'
+ pd='2*int((nf+1)/2) * (W/nf + 0.29)' ps='2*int((nf+2)/2) * (W/nf + 0.29)' nrd='0.29 / W' nrs='0.29 / W'
+ sa=0 sb=0 sd=0 mult=1 m=1
XM2b VP Vbp Vcn VDD sky130_fd_pr__pfet_01v8 L=0.5 W=6 nf=1 ad='int((nf+1)/2) * W/nf * 0.29' as='int((nf+2)/2) * W/nf * 0.29'
+ pd='2*int((nf+1)/2) * (W/nf + 0.29)' ps='2*int((nf+2)/2) * (W/nf + 0.29)' nrd='0.29 / W' nrs='0.29 / W'
+ sa=0 sb=0 sd=0 mult=1 m=1
XM9a net11 Vcp Vcp VDD sky130_fd_pr__pfet_01v8 L=0.5 W=6 nf=1 ad='int((nf+1)/2) * W/nf * 0.29' as='int((nf+2)/2) * W/nf * 0.29'
+ pd='2*int((nf+1)/2) * (W/nf + 0.29)' ps='2*int((nf+2)/2) * (W/nf + 0.29)' nrd='0.29 / W' nrs='0.29 / W'
+ sa=0 sb=0 sd=0 mult=1 m=1
XM8a net12 net12 net11 VDD sky130_fd_pr__pfet_01v8 L=0.5 W=6 nf=1 ad='int((nf+1)/2) * W/nf * 0.29' as='int((nf+2)/2) * W/nf * 0.29'
+ pd='2*int((nf+1)/2) * (W/nf + 0.29)' ps='2*int((nf+2)/2) * (W/nf + 0.29)' nrd='0.29 / W' nrs='0.29 / W'
+ sa=0 sb=0 sd=0 mult=1 m=1
XM8b net11 net12 net12 VDD sky130_fd_pr__pfet_01v8 L=0.5 W=6 nf=1 ad='int((nf+1)/2) * W/nf * 0.29' as='int((nf+2)/2) * W/nf * 0.29'
+ pd='2*int((nf+1)/2) * (W/nf + 0.29)' ps='2*int((nf+2)/2) * (W/nf + 0.29)' nrd='0.29 / W' nrs='0.29 / W'
+ sa=0 sb=0 sd=0 mult=1 m=1
XM8c net12 net12 net11 VDD sky130_fd_pr__pfet_01v8 L=0.5 W=6 nf=1 ad='int((nf+1)/2) * W/nf * 0.29' as='int((nf+2)/2) * W/nf * 0.29'
+ pd='2*int((nf+1)/2) * (W/nf + 0.29)' ps='2*int((nf+2)/2) * (W/nf + 0.29)' nrd='0.29 / W' nrs='0.29 / W'
+ sa=0 sb=0 sd=0 mult=1 m=1
XM8d net11 net12 net12 VDD sky130_fd_pr__pfet_01v8 L=0.5 W=6 nf=1 ad='int((nf+1)/2) * W/nf * 0.29' as='int((nf+2)/2) * W/nf * 0.29'
+ pd='2*int((nf+1)/2) * (W/nf + 0.29)' ps='2*int((nf+2)/2) * (W/nf + 0.29)' nrd='0.29 / W' nrs='0.29 / W'
+ sa=0 sb=0 sd=0 mult=1 m=1
XM10a VP net12 net11 VDD sky130_fd_pr__pfet_01v8 L=0.5 W=6 nf=1 ad='int((nf+1)/2) * W/nf * 0.29' as='int((nf+2)/2) * W/nf * 0.29'
+ pd='2*int((nf+1)/2) * (W/nf + 0.29)' ps='2*int((nf+2)/2) * (W/nf + 0.29)' nrd='0.29 / W' nrs='0.29 / W'
+ sa=0 sb=0 sd=0 mult=1 m=1
XM11a VP Vbp Vbp VDD sky130_fd_pr__pfet_01v8 L=0.5 W=6 nf=1 ad='int((nf+1)/2) * W/nf * 0.29' as='int((nf+2)/2) * W/nf * 0.29'
+ pd='2*int((nf+1)/2) * (W/nf + 0.29)' ps='2*int((nf+2)/2) * (W/nf + 0.29)' nrd='0.29 / W' nrs='0.29 / W'
+ sa=0 sb=0 sd=0 mult=1 m=1
XM11b Vbp Vbp VP VDD sky130_fd_pr__pfet_01v8 L=0.5 W=6 nf=1 ad='int((nf+1)/2) * W/nf * 0.29' as='int((nf+2)/2) * W/nf * 0.29'
+ pd='2*int((nf+1)/2) * (W/nf + 0.29)' ps='2*int((nf+2)/2) * (W/nf + 0.29)' nrd='0.29 / W' nrs='0.29 / W'
+ sa=0 sb=0 sd=0 mult=1 m=1
XM10b net11 net12 VP VDD sky130_fd_pr__pfet_01v8 L=0.5 W=6 nf=1 ad='int((nf+1)/2) * W/nf * 0.29' as='int((nf+2)/2) * W/nf * 0.29'
+ pd='2*int((nf+1)/2) * (W/nf + 0.29)' ps='2*int((nf+2)/2) * (W/nf + 0.29)' nrd='0.29 / W' nrs='0.29 / W'
+ sa=0 sb=0 sd=0 mult=1 m=1
XM8e net12 net12 net11 VDD sky130_fd_pr__pfet_01v8 L=0.5 W=6 nf=1 ad='int((nf+1)/2) * W/nf * 0.29' as='int((nf+2)/2) * W/nf * 0.29'
+ pd='2*int((nf+1)/2) * (W/nf + 0.29)' ps='2*int((nf+2)/2) * (W/nf + 0.29)' nrd='0.29 / W' nrs='0.29 / W'
+ sa=0 sb=0 sd=0 mult=1 m=1
XM8f net11 net12 net12 VDD sky130_fd_pr__pfet_01v8 L=0.5 W=6 nf=1 ad='int((nf+1)/2) * W/nf * 0.29' as='int((nf+2)/2) * W/nf * 0.29'
+ pd='2*int((nf+1)/2) * (W/nf + 0.29)' ps='2*int((nf+2)/2) * (W/nf + 0.29)' nrd='0.29 / W' nrs='0.29 / W'
+ sa=0 sb=0 sd=0 mult=1 m=1
XM8g net12 net12 net11 VDD sky130_fd_pr__pfet_01v8 L=0.5 W=6 nf=1 ad='int((nf+1)/2) * W/nf * 0.29' as='int((nf+2)/2) * W/nf * 0.29'
+ pd='2*int((nf+1)/2) * (W/nf + 0.29)' ps='2*int((nf+2)/2) * (W/nf + 0.29)' nrd='0.29 / W' nrs='0.29 / W'
+ sa=0 sb=0 sd=0 mult=1 m=1
XM8h net11 net12 net12 VDD sky130_fd_pr__pfet_01v8 L=0.5 W=6 nf=1 ad='int((nf+1)/2) * W/nf * 0.29' as='int((nf+2)/2) * W/nf * 0.29'
+ pd='2*int((nf+1)/2) * (W/nf + 0.29)' ps='2*int((nf+2)/2) * (W/nf + 0.29)' nrd='0.29 / W' nrs='0.29 / W'
+ sa=0 sb=0 sd=0 mult=1 m=1
XM9b Vcp Vcp net11 VDD sky130_fd_pr__pfet_01v8 L=0.5 W=6 nf=1 ad='int((nf+1)/2) * W/nf * 0.29' as='int((nf+2)/2) * W/nf * 0.29'
+ pd='2*int((nf+1)/2) * (W/nf + 0.29)' ps='2*int((nf+2)/2) * (W/nf + 0.29)' nrd='0.29 / W' nrs='0.29 / W'
+ sa=0 sb=0 sd=0 mult=1 m=1
XM4a net13 Vcn Vcn GND sky130_fd_pr__nfet_01v8 L=0.5 W=6 nf=1 ad='int((nf+1)/2) * W/nf * 0.29' as='int((nf+2)/2) * W/nf * 0.29'
+ pd='2*int((nf+1)/2) * (W/nf + 0.29)' ps='2*int((nf+2)/2) * (W/nf + 0.29)' nrd='0.29 / W' nrs='0.29 / W'
+ sa=0 sb=0 sd=0 mult=1 m=1
XM3a net14 net14 net13 GND sky130_fd_pr__nfet_01v8 L=0.5 W=6 nf=1 ad='int((nf+1)/2) * W/nf * 0.29' as='int((nf+2)/2) * W/nf * 0.29'
+ pd='2*int((nf+1)/2) * (W/nf + 0.29)' ps='2*int((nf+2)/2) * (W/nf + 0.29)' nrd='0.29 / W' nrs='0.29 / W'
+ sa=0 sb=0 sd=0 mult=1 m=1
XM3b net13 net14 net14 GND sky130_fd_pr__nfet_01v8 L=0.5 W=6 nf=1 ad='int((nf+1)/2) * W/nf * 0.29' as='int((nf+2)/2) * W/nf * 0.29'
+ pd='2*int((nf+1)/2) * (W/nf + 0.29)' ps='2*int((nf+2)/2) * (W/nf + 0.29)' nrd='0.29 / W' nrs='0.29 / W'
+ sa=0 sb=0 sd=0 mult=1 m=1
XM3c net14 net14 net13 GND sky130_fd_pr__nfet_01v8 L=0.5 W=6 nf=1 ad='int((nf+1)/2) * W/nf * 0.29' as='int((nf+2)/2) * W/nf * 0.29'
+ pd='2*int((nf+1)/2) * (W/nf + 0.29)' ps='2*int((nf+2)/2) * (W/nf + 0.29)' nrd='0.29 / W' nrs='0.29 / W'
+ sa=0 sb=0 sd=0 mult=1 m=1
XM3d net13 net14 net14 GND sky130_fd_pr__nfet_01v8 L=0.5 W=6 nf=1 ad='int((nf+1)/2) * W/nf * 0.29' as='int((nf+2)/2) * W/nf * 0.29'
+ pd='2*int((nf+1)/2) * (W/nf + 0.29)' ps='2*int((nf+2)/2) * (W/nf + 0.29)' nrd='0.29 / W' nrs='0.29 / W'
+ sa=0 sb=0 sd=0 mult=1 m=1
XM5a VN net14 net13 GND sky130_fd_pr__nfet_01v8 L=0.5 W=6 nf=1 ad='int((nf+1)/2) * W/nf * 0.29' as='int((nf+2)/2) * W/nf * 0.29'
+ pd='2*int((nf+1)/2) * (W/nf + 0.29)' ps='2*int((nf+2)/2) * (W/nf + 0.29)' nrd='0.29 / W' nrs='0.29 / W'
+ sa=0 sb=0 sd=0 mult=1 m=1
XM12a VN Vbn Vbp GND sky130_fd_pr__nfet_01v8 L=0.5 W=6 nf=1 ad='int((nf+1)/2) * W/nf * 0.29' as='int((nf+2)/2) * W/nf * 0.29'
+ pd='2*int((nf+1)/2) * (W/nf + 0.29)' ps='2*int((nf+2)/2) * (W/nf + 0.29)' nrd='0.29 / W' nrs='0.29 / W'
+ sa=0 sb=0 sd=0 mult=1 m=1
XM12b Vbp Vbn VN GND sky130_fd_pr__nfet_01v8 L=0.5 W=6 nf=1 ad='int((nf+1)/2) * W/nf * 0.29' as='int((nf+2)/2) * W/nf * 0.29'
+ pd='2*int((nf+1)/2) * (W/nf + 0.29)' ps='2*int((nf+2)/2) * (W/nf + 0.29)' nrd='0.29 / W' nrs='0.29 / W'
+ sa=0 sb=0 sd=0 mult=1 m=1
XM5b net13 net14 VN GND sky130_fd_pr__nfet_01v8 L=0.5 W=6 nf=1 ad='int((nf+1)/2) * W/nf * 0.29' as='int((nf+2)/2) * W/nf * 0.29'
+ pd='2*int((nf+1)/2) * (W/nf + 0.29)' ps='2*int((nf+2)/2) * (W/nf + 0.29)' nrd='0.29 / W' nrs='0.29 / W'
+ sa=0 sb=0 sd=0 mult=1 m=1
XM3e net14 net14 net13 GND sky130_fd_pr__nfet_01v8 L=0.5 W=6 nf=1 ad='int((nf+1)/2) * W/nf * 0.29' as='int((nf+2)/2) * W/nf * 0.29'
+ pd='2*int((nf+1)/2) * (W/nf + 0.29)' ps='2*int((nf+2)/2) * (W/nf + 0.29)' nrd='0.29 / W' nrs='0.29 / W'
+ sa=0 sb=0 sd=0 mult=1 m=1
XM3f net13 net14 net14 GND sky130_fd_pr__nfet_01v8 L=0.5 W=6 nf=1 ad='int((nf+1)/2) * W/nf * 0.29' as='int((nf+2)/2) * W/nf * 0.29'
+ pd='2*int((nf+1)/2) * (W/nf + 0.29)' ps='2*int((nf+2)/2) * (W/nf + 0.29)' nrd='0.29 / W' nrs='0.29 / W'
+ sa=0 sb=0 sd=0 mult=1 m=1
XM3g net14 net14 net13 GND sky130_fd_pr__nfet_01v8 L=0.5 W=6 nf=1 ad='int((nf+1)/2) * W/nf * 0.29' as='int((nf+2)/2) * W/nf * 0.29'
+ pd='2*int((nf+1)/2) * (W/nf + 0.29)' ps='2*int((nf+2)/2) * (W/nf + 0.29)' nrd='0.29 / W' nrs='0.29 / W'
+ sa=0 sb=0 sd=0 mult=1 m=1
XM3h net13 net14 net14 GND sky130_fd_pr__nfet_01v8 L=0.5 W=6 nf=1 ad='int((nf+1)/2) * W/nf * 0.29' as='int((nf+2)/2) * W/nf * 0.29'
+ pd='2*int((nf+1)/2) * (W/nf + 0.29)' ps='2*int((nf+2)/2) * (W/nf + 0.29)' nrd='0.29 / W' nrs='0.29 / W'
+ sa=0 sb=0 sd=0 mult=1 m=1
XM4b Vcn Vcn net13 GND sky130_fd_pr__nfet_01v8 L=0.5 W=6 nf=1 ad='int((nf+1)/2) * W/nf * 0.29' as='int((nf+2)/2) * W/nf * 0.29'
+ pd='2*int((nf+1)/2) * (W/nf + 0.29)' ps='2*int((nf+2)/2) * (W/nf + 0.29)' nrd='0.29 / W' nrs='0.29 / W'
+ sa=0 sb=0 sd=0 mult=1 m=1
XM7a Vcp Vbn VN GND sky130_fd_pr__nfet_01v8 L=0.5 W=6 nf=1 ad='int((nf+1)/2) * W/nf * 0.29' as='int((nf+2)/2) * W/nf * 0.29'
+ pd='2*int((nf+1)/2) * (W/nf + 0.29)' ps='2*int((nf+2)/2) * (W/nf + 0.29)' nrd='0.29 / W' nrs='0.29 / W'
+ sa=0 sb=0 sd=0 mult=1 m=1
XM6a VN Vbn net15 GND sky130_fd_pr__nfet_01v8 L=0.5 W=6 nf=1 ad='int((nf+1)/2) * W/nf * 0.29' as='int((nf+2)/2) * W/nf * 0.29'
+ pd='2*int((nf+1)/2) * (W/nf + 0.29)' ps='2*int((nf+2)/2) * (W/nf + 0.29)' nrd='0.29 / W' nrs='0.29 / W'
+ sa=0 sb=0 sd=0 mult=1 m=1
XM6b net15 Vbn net16 GND sky130_fd_pr__nfet_01v8 L=0.5 W=6 nf=1 ad='int((nf+1)/2) * W/nf * 0.29' as='int((nf+2)/2) * W/nf * 0.29'
+ pd='2*int((nf+1)/2) * (W/nf + 0.29)' ps='2*int((nf+2)/2) * (W/nf + 0.29)' nrd='0.29 / W' nrs='0.29 / W'
+ sa=0 sb=0 sd=0 mult=1 m=1
XM6c net16 Vbn net17 GND sky130_fd_pr__nfet_01v8 L=0.5 W=6 nf=1 ad='int((nf+1)/2) * W/nf * 0.29' as='int((nf+2)/2) * W/nf * 0.29'
+ pd='2*int((nf+1)/2) * (W/nf + 0.29)' ps='2*int((nf+2)/2) * (W/nf + 0.29)' nrd='0.29 / W' nrs='0.29 / W'
+ sa=0 sb=0 sd=0 mult=1 m=1
XM6d net17 Vbn net18 GND sky130_fd_pr__nfet_01v8 L=0.5 W=6 nf=1 ad='int((nf+1)/2) * W/nf * 0.29' as='int((nf+2)/2) * W/nf * 0.29'
+ pd='2*int((nf+1)/2) * (W/nf + 0.29)' ps='2*int((nf+2)/2) * (W/nf + 0.29)' nrd='0.29 / W' nrs='0.29 / W'
+ sa=0 sb=0 sd=0 mult=1 m=1
XM6e net18 Vbn net19 GND sky130_fd_pr__nfet_01v8 L=0.5 W=6 nf=1 ad='int((nf+1)/2) * W/nf * 0.29' as='int((nf+2)/2) * W/nf * 0.29'
+ pd='2*int((nf+1)/2) * (W/nf + 0.29)' ps='2*int((nf+2)/2) * (W/nf + 0.29)' nrd='0.29 / W' nrs='0.29 / W'
+ sa=0 sb=0 sd=0 mult=1 m=1
XM6f net19 Vbn net12 GND sky130_fd_pr__nfet_01v8 L=0.5 W=6 nf=1 ad='int((nf+1)/2) * W/nf * 0.29' as='int((nf+2)/2) * W/nf * 0.29'
+ pd='2*int((nf+1)/2) * (W/nf + 0.29)' ps='2*int((nf+2)/2) * (W/nf + 0.29)' nrd='0.29 / W' nrs='0.29 / W'
+ sa=0 sb=0 sd=0 mult=1 m=1
XM6g net12 Vbn net20 GND sky130_fd_pr__nfet_01v8 L=0.5 W=6 nf=1 ad='int((nf+1)/2) * W/nf * 0.29' as='int((nf+2)/2) * W/nf * 0.29'
+ pd='2*int((nf+1)/2) * (W/nf + 0.29)' ps='2*int((nf+2)/2) * (W/nf + 0.29)' nrd='0.29 / W' nrs='0.29 / W'
+ sa=0 sb=0 sd=0 mult=1 m=1
XM6h net20 Vbn net21 GND sky130_fd_pr__nfet_01v8 L=0.5 W=6 nf=1 ad='int((nf+1)/2) * W/nf * 0.29' as='int((nf+2)/2) * W/nf * 0.29'
+ pd='2*int((nf+1)/2) * (W/nf + 0.29)' ps='2*int((nf+2)/2) * (W/nf + 0.29)' nrd='0.29 / W' nrs='0.29 / W'
+ sa=0 sb=0 sd=0 mult=1 m=1
XM6i net21 Vbn net22 GND sky130_fd_pr__nfet_01v8 L=0.5 W=6 nf=1 ad='int((nf+1)/2) * W/nf * 0.29' as='int((nf+2)/2) * W/nf * 0.29'
+ pd='2*int((nf+1)/2) * (W/nf + 0.29)' ps='2*int((nf+2)/2) * (W/nf + 0.29)' nrd='0.29 / W' nrs='0.29 / W'
+ sa=0 sb=0 sd=0 mult=1 m=1
XM6j net22 Vbn net23 GND sky130_fd_pr__nfet_01v8 L=0.5 W=6 nf=1 ad='int((nf+1)/2) * W/nf * 0.29' as='int((nf+2)/2) * W/nf * 0.29'
+ pd='2*int((nf+1)/2) * (W/nf + 0.29)' ps='2*int((nf+2)/2) * (W/nf + 0.29)' nrd='0.29 / W' nrs='0.29 / W'
+ sa=0 sb=0 sd=0 mult=1 m=1
XM6k net23 Vbn net24 GND sky130_fd_pr__nfet_01v8 L=0.5 W=6 nf=1 ad='int((nf+1)/2) * W/nf * 0.29' as='int((nf+2)/2) * W/nf * 0.29'
+ pd='2*int((nf+1)/2) * (W/nf + 0.29)' ps='2*int((nf+2)/2) * (W/nf + 0.29)' nrd='0.29 / W' nrs='0.29 / W'
+ sa=0 sb=0 sd=0 mult=1 m=1
XM6l net24 Vbn VN GND sky130_fd_pr__nfet_01v8 L=0.5 W=6 nf=1 ad='int((nf+1)/2) * W/nf * 0.29' as='int((nf+2)/2) * W/nf * 0.29'
+ pd='2*int((nf+1)/2) * (W/nf + 0.29)' ps='2*int((nf+2)/2) * (W/nf + 0.29)' nrd='0.29 / W' nrs='0.29 / W'
+ sa=0 sb=0 sd=0 mult=1 m=1
XM7b VN Vbn Vcp GND sky130_fd_pr__nfet_01v8 L=0.5 W=6 nf=1 ad='int((nf+1)/2) * W/nf * 0.29' as='int((nf+2)/2) * W/nf * 0.29'
+ pd='2*int((nf+1)/2) * (W/nf + 0.29)' ps='2*int((nf+2)/2) * (W/nf + 0.29)' nrd='0.29 / W' nrs='0.29 / W'
+ sa=0 sb=0 sd=0 mult=1 m=1
XM17 Vcn VP VP VDD sky130_fd_pr__pfet_01v8 L=0.5 W=6 nf=1 ad='int((nf+1)/2) * W/nf * 0.29' as='int((nf+2)/2) * W/nf * 0.29'
+ pd='2*int((nf+1)/2) * (W/nf + 0.29)' ps='2*int((nf+2)/2) * (W/nf + 0.29)' nrd='0.29 / W' nrs='0.29 / W'
+ sa=0 sb=0 sd=0 mult=1 m=1
XM18 VP VP Vcp VDD sky130_fd_pr__pfet_01v8 L=0.5 W=6 nf=1 ad='int((nf+1)/2) * W/nf * 0.29' as='int((nf+2)/2) * W/nf * 0.29'
+ pd='2*int((nf+1)/2) * (W/nf + 0.29)' ps='2*int((nf+2)/2) * (W/nf + 0.29)' nrd='0.29 / W' nrs='0.29 / W'
+ sa=0 sb=0 sd=0 mult=1 m=1
XM13 VN VN Vcn GND sky130_fd_pr__nfet_01v8 L=0.5 W=6 nf=1 ad='int((nf+1)/2) * W/nf * 0.29' as='int((nf+2)/2) * W/nf * 0.29'
+ pd='2*int((nf+1)/2) * (W/nf + 0.29)' ps='2*int((nf+2)/2) * (W/nf + 0.29)' nrd='0.29 / W' nrs='0.29 / W'
+ sa=0 sb=0 sd=0 mult=1 m=1
XM14 Vcp VN VN GND sky130_fd_pr__nfet_01v8 L=0.5 W=6 nf=1 ad='int((nf+1)/2) * W/nf * 0.29' as='int((nf+2)/2) * W/nf * 0.29'
+ pd='2*int((nf+1)/2) * (W/nf + 0.29)' ps='2*int((nf+2)/2) * (W/nf + 0.29)' nrd='0.29 / W' nrs='0.29 / W'
+ sa=0 sb=0 sd=0 mult=1 m=1
XM19 Vcn VP VP VDD sky130_fd_pr__pfet_01v8 L=0.5 W=6 nf=1 ad='int((nf+1)/2) * W/nf * 0.29' as='int((nf+2)/2) * W/nf * 0.29'
+ pd='2*int((nf+1)/2) * (W/nf + 0.29)' ps='2*int((nf+2)/2) * (W/nf + 0.29)' nrd='0.29 / W' nrs='0.29 / W'
+ sa=0 sb=0 sd=0 mult=1 m=1
XM20 Vcp VP VP VDD sky130_fd_pr__pfet_01v8 L=0.5 W=6 nf=1 ad='int((nf+1)/2) * W/nf * 0.29' as='int((nf+2)/2) * W/nf * 0.29'
+ pd='2*int((nf+1)/2) * (W/nf + 0.29)' ps='2*int((nf+2)/2) * (W/nf + 0.29)' nrd='0.29 / W' nrs='0.29 / W'
+ sa=0 sb=0 sd=0 mult=1 m=1
XM15 Vcn VN VN GND sky130_fd_pr__nfet_01v8 L=0.5 W=6 nf=1 ad='int((nf+1)/2) * W/nf * 0.29' as='int((nf+2)/2) * W/nf * 0.29'
+ pd='2*int((nf+1)/2) * (W/nf + 0.29)' ps='2*int((nf+2)/2) * (W/nf + 0.29)' nrd='0.29 / W' nrs='0.29 / W'
+ sa=0 sb=0 sd=0 mult=1 m=1
XM16 Vcp VN VN GND sky130_fd_pr__nfet_01v8 L=0.5 W=6 nf=1 ad='int((nf+1)/2) * W/nf * 0.29' as='int((nf+2)/2) * W/nf * 0.29'
+ pd='2*int((nf+1)/2) * (W/nf + 0.29)' ps='2*int((nf+2)/2) * (W/nf + 0.29)' nrd='0.29 / W' nrs='0.29 / W'
+ sa=0 sb=0 sd=0 mult=1 m=1
.ends

.GLOBAL GND
.GLOBAL VDD
.end
